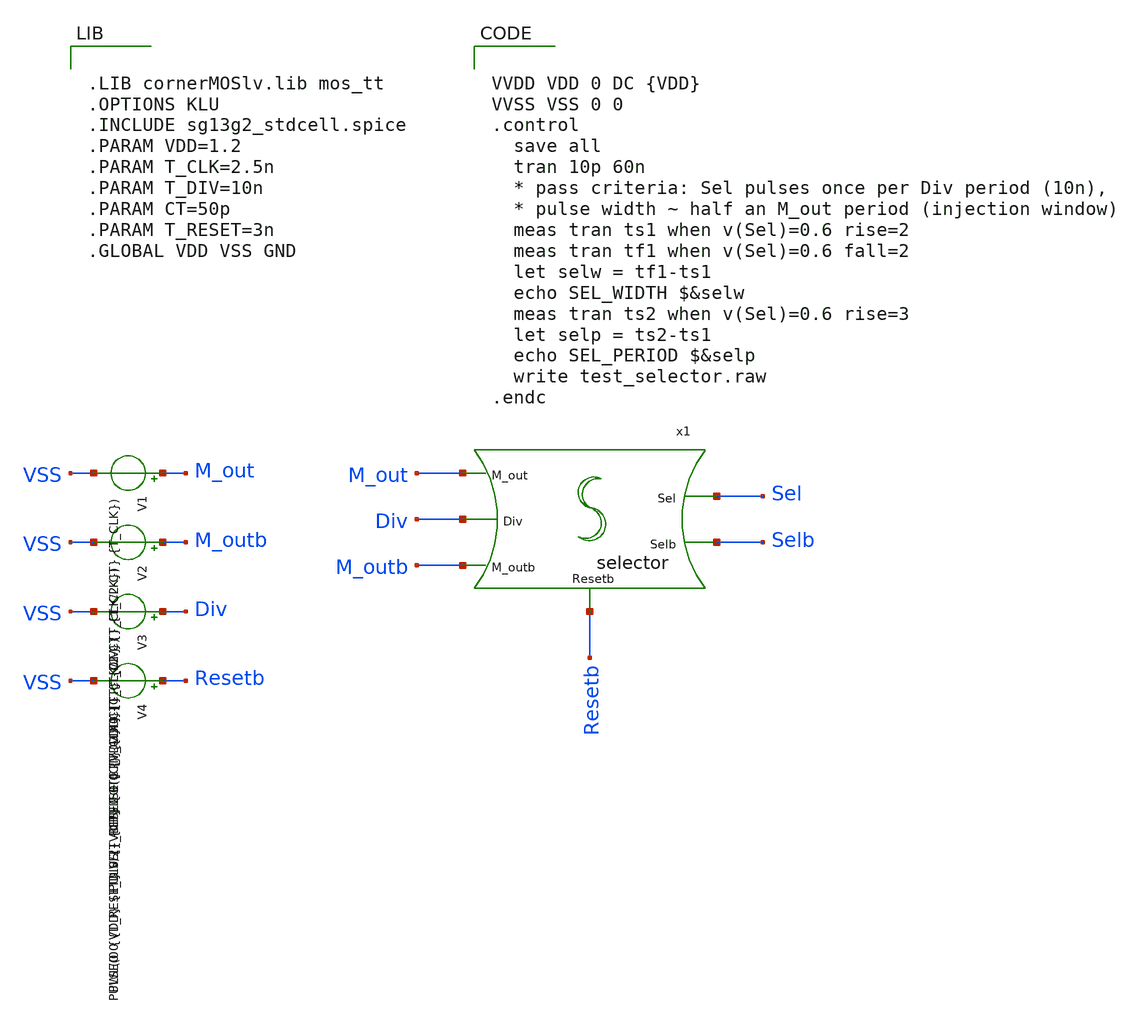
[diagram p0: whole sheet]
** sch_path: TPU5555-main/mdll/mixed_signal_design_blocks/clk_gen/test_selector.sch


.LIB cornerMOSlv.lib mos_tt
.OPTIONS KLU
.INCLUDE sg13g2_stdcell.spice
.PARAM VDD=1.2
.PARAM T_CLK=2.5n
.PARAM T_DIV=10n
.PARAM CT=50p
.PARAM T_RESET=3n
.GLOBAL VDD VSS GND


**.subckt test_selector
x1 M_outb Sel Div Resetb M_out Selb selector
V1 M_out VSS PULSE(0 {VDD} 0 {CT} {CT} {T_CLK/2-CT} {T_CLK})
V2 M_outb VSS PULSE({VDD} 0 0 {CT} {CT} {T_CLK/2-CT} {T_CLK})
V3 Div VSS PULSE(0 {VDD} {T_DIV/2} {CT} {CT} {T_CLK-CT} {T_DIV})
V4 Resetb VSS PWL(0 0 {T_RESET} 0 {T_RESET + CT} {VDD})
**** begin user architecture code


VVDD VDD 0 DC {VDD}
VVSS VSS 0 0
.control
  save all
  tran 10p 60n
  * pass criteria: Sel pulses once per Div period (10n),
  * pulse width ~ half an M_out period (injection window)
  meas tran ts1 when v(Sel)=0.6 rise=2
  meas tran tf1 when v(Sel)=0.6 fall=2
  let selw = tf1-ts1
  echo SEL_WIDTH $&selw
  meas tran ts2 when v(Sel)=0.6 rise=3
  let selp = ts2-ts1
  echo SEL_PERIOD $&selp
  write test_selector.raw
.endc


**** end user architecture code
**.ends
.end
